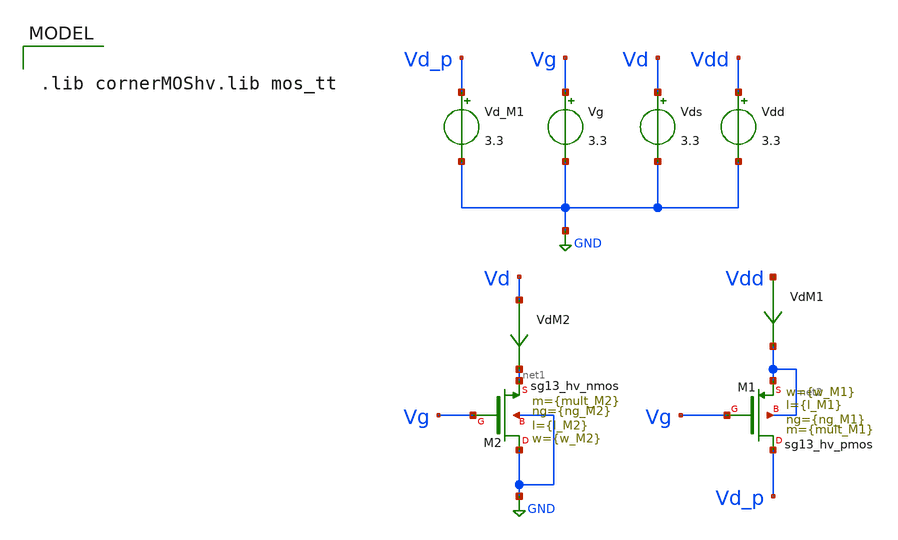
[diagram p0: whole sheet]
** sch_path: xschem/TB_hvMOS_POWER_Sizing.sch
**.subckt TB_hvMOS_POWER_Sizing
Vg Vg GND 3.3
Vds Vd GND 3.3
Vdd Vdd GND 3.3
XM2 GND Vg net1 GND sg13_hv_nmos w={w_M2} l={l_M2} ng={ng_M2} m={mult_M2} mm_ok=1
VdM1 Vdd net2 0
.save i(vdm1)
XM1 Vd_p Vg net2 net2 sg13_hv_pmos w={w_M1} l={l_M1} ng={ng_M1} m={mult_M1} mm_ok=1
VdM2 Vd net1 0
.save i(vdm2)
Vd_M1 Vd_p GND 3.3
**** begin user architecture code

.lib cornerMOShv.lib mos_tt



.save all
* + @M.XM1.m1[id]  @n.xm1.nsg13_hv_pmos[vth]  @n.xm1.nsg13_hv_pmos[gds]  @n.xm1.nsg13_hv_pmos[ad]
*+  @n.xm2.nsg13_hv_nmos[vth]  @n.xm2.nsg13_hv_nmos[gds]

.control
reset
alter Vg 3.3
dc Vds 0 0.5 0.01
*dc Vds 0 0.5 0.01 temp 0 27 1
let Vds_M2 = v(Vd)
plot i(VdM2) vs Vds_M2

let G_M2 = @n.xm2.nsg13_hv_nmos[gds]
let Ron_M2 = 1/G_M2
let I_M2 = i(VdM2)
let G_M22 = deriv(I_M2)
let Ron_M22 = 1/G_M22

plot Ron_M2 vs Vds_M2

*let VthM1_off =  @n.xm1.nsg13_hv_pmos[vth]
*let VthM2 =  @n.xm2.nsg13_hv_nmos[vth]
*plot VthM1_off
*plot VthM2
.endc

.control
reset
alter Vg 0
dc Vd_M1 2.5 3.3 0.01
*dc Vd_M1 2 3.3 0.01 temp 0 27 1

let Vsd_M1 = v(Vdd) -v(Vd_p)
plot i(VdM1) vs Vsd_M1
let G_M1 = @n.xm1.nsg13_hv_pmos[gds]
let Ron_M1 = 1/G_M1
let I_M1 = i(VdM1)
let G_M11 = deriv(I_M1)
let Ron_M11 = -1/G_M11

plot Ron_M1 vs Vsd_M1

*plot Ron_M11
*plot Ron_M11 vs Vsd_M1
*let VthM1_on = @n.xm1.nsg13_hv_pmos[vth]
*plot VthM1_on
.endc

.control
reset
alter Vg 3.3
dc Vd_M1 0 3.3 0.01
let Vsd_M1 = v(Vdd) -v(Vd_p)
*plot i(VdM1) vs Vsd_M1
let G_M1 = @n.xm1.nsg13_hv_pmos[gds]
let I_M1 = i(VdM1)


let VthM1_subth = @n.xm1.nsg13_hv_pmos[vth]
*plot VthM1_subth
.endc
.end




.param temp=27
.param mult_M1 = 2400
.param w_M1 =10u
*.param l_M1 = 0.2u ** Posee mayor capacidad de corriente, pero en sub-umbral conduce mucha
*+ corriente
.param l_M1 = 0.22u
.param ng_M1 = 1

.param mult_M2 = 1200
.param w_M2 =10u
.param l_M2 =0.25u
.param ng_M2 =1





**** end user architecture code
**.ends
.GLOBAL GND
.end
